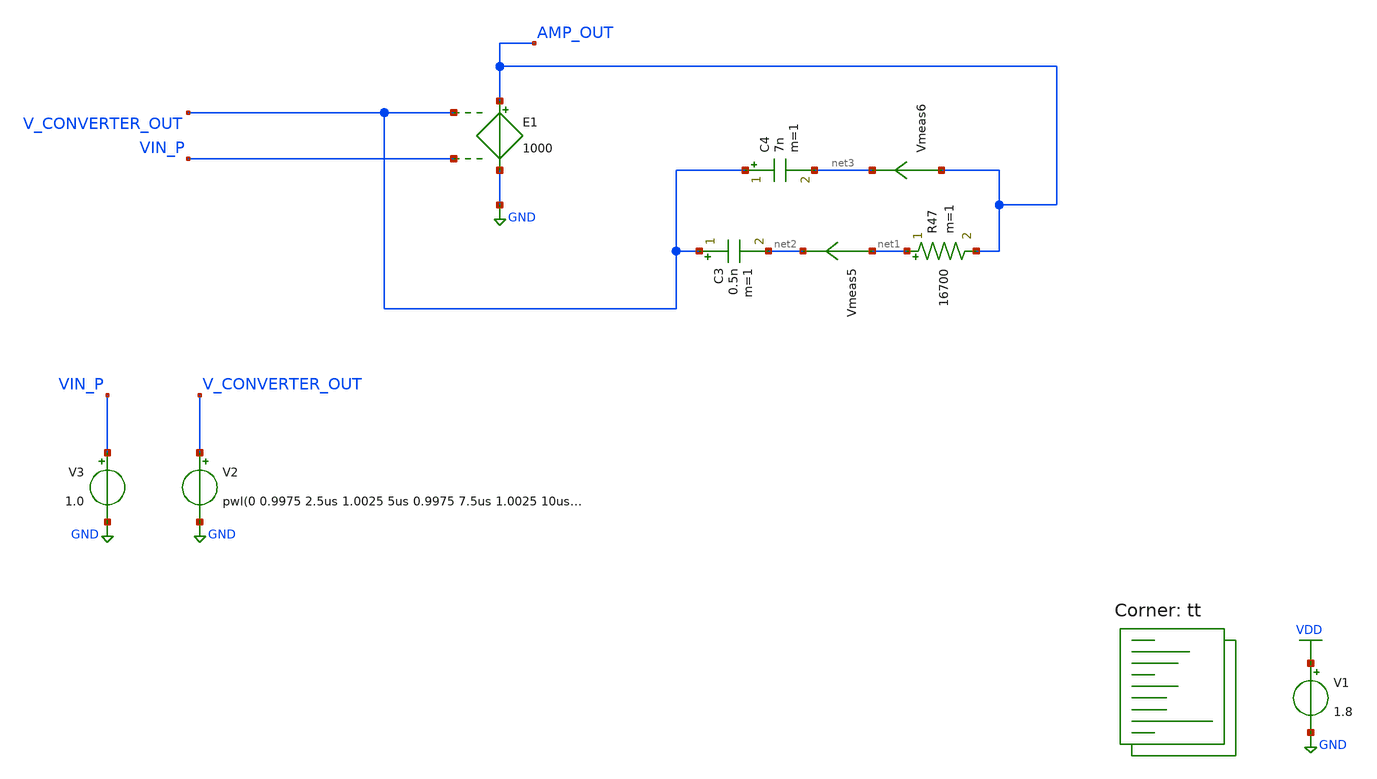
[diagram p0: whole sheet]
** sch_path: projects/ASU/EEE572/schematic/tb_vcvs.sch
**.subckt tb_vcvs
V1 VDD GND 1.8
V2 V_CONVERTER_OUT GND pwl(0 0.9975 2.5us 1.0025 5us 0.9975 7.5us 1.0025 10us 0.9975 12.5us 1.0025
+ 15us 0.9975 17.5us 1.0025 20us 0.9975 22.5us 1.0025 25us 0.9975)
V3 VIN_P GND 1.0
E1 AMP_OUT GND V_CONVERTER_OUT VIN_P 1000
C3 V_CONVERTER_OUT net2 0.5n m=1
R47 net1 AMP_OUT 16700 m=1
C4 V_CONVERTER_OUT net3 7n m=1
Vmeas5 net1 net2 0
.save i(vmeas5)
Vmeas6 AMP_OUT net3 0
.save i(vmeas6)
**** begin user architecture code
.lib $::SKYWATER_MODELS/sky130.lib.spice tt



.options method=gear
.options wnflag=1
* .options savecurrents

.control

  * save v(vin_p) v(vin_m) v(int_btw) v(v_converter_out) v(amp_out) v(ph(amp_out))
  save all
  * tran 0.1ns 4us
  * tran 0.01ns 0.4us
  tran 100ps 25us
  remzerovec
  write tb_vcvs.raw
  set appendwrite

.endc




**** end user architecture code
**.ends
.GLOBAL GND
.GLOBAL VDD
.end
